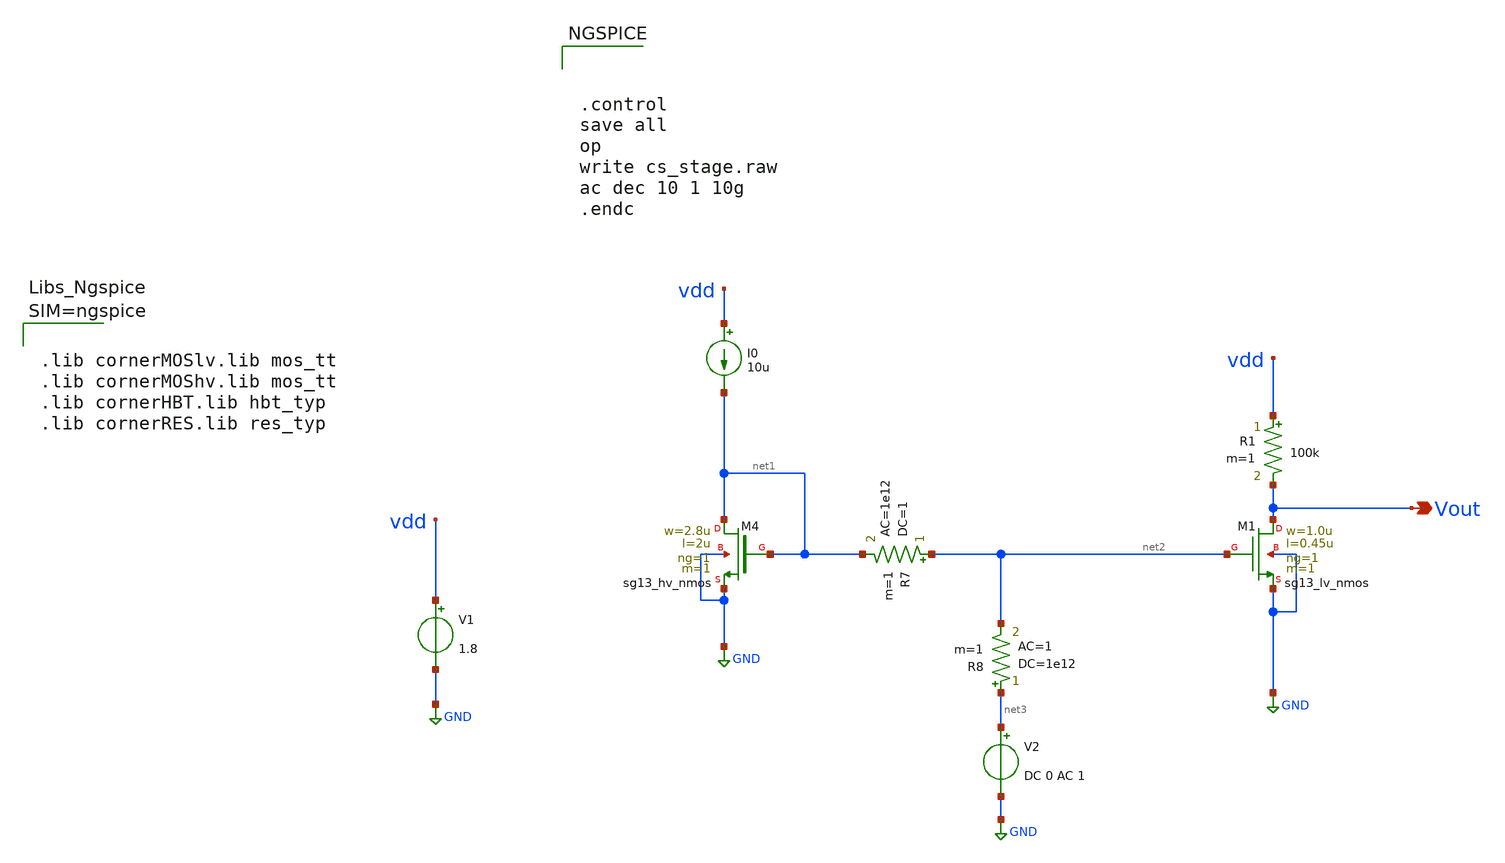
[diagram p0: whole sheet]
** sch_path: Schematics/cs_stage.sch
**.subckt cs_stage Vout
*.opin Vout
V1 vdd GND 1.8
R1 vdd Vout 100k m=1
I0 vdd net1 10u
XM4 net1 net1 GND GND sg13_hv_nmos w=2.8u l=2u ng=1 m=1 mm_ok=1
R7 net2 net1 1 ac=1e12 m=1
R8 net3 net2 1e12 ac=1 m=1
V2 net3 GND DC 0 AC 1
XM1 Vout net2 GND GND sg13_lv_nmos w=1.0u l=0.45u ng=1 m=1 mm_ok=1
**** begin user architecture code



.lib cornerMOSlv.lib mos_tt
.lib cornerMOShv.lib mos_tt
.lib cornerHBT.lib hbt_typ
.lib cornerRES.lib res_typ






.control
save all
op
write cs_stage.raw
ac dec 10 1 10g
.endc


**** end user architecture code
**.ends
.GLOBAL GND
.end
